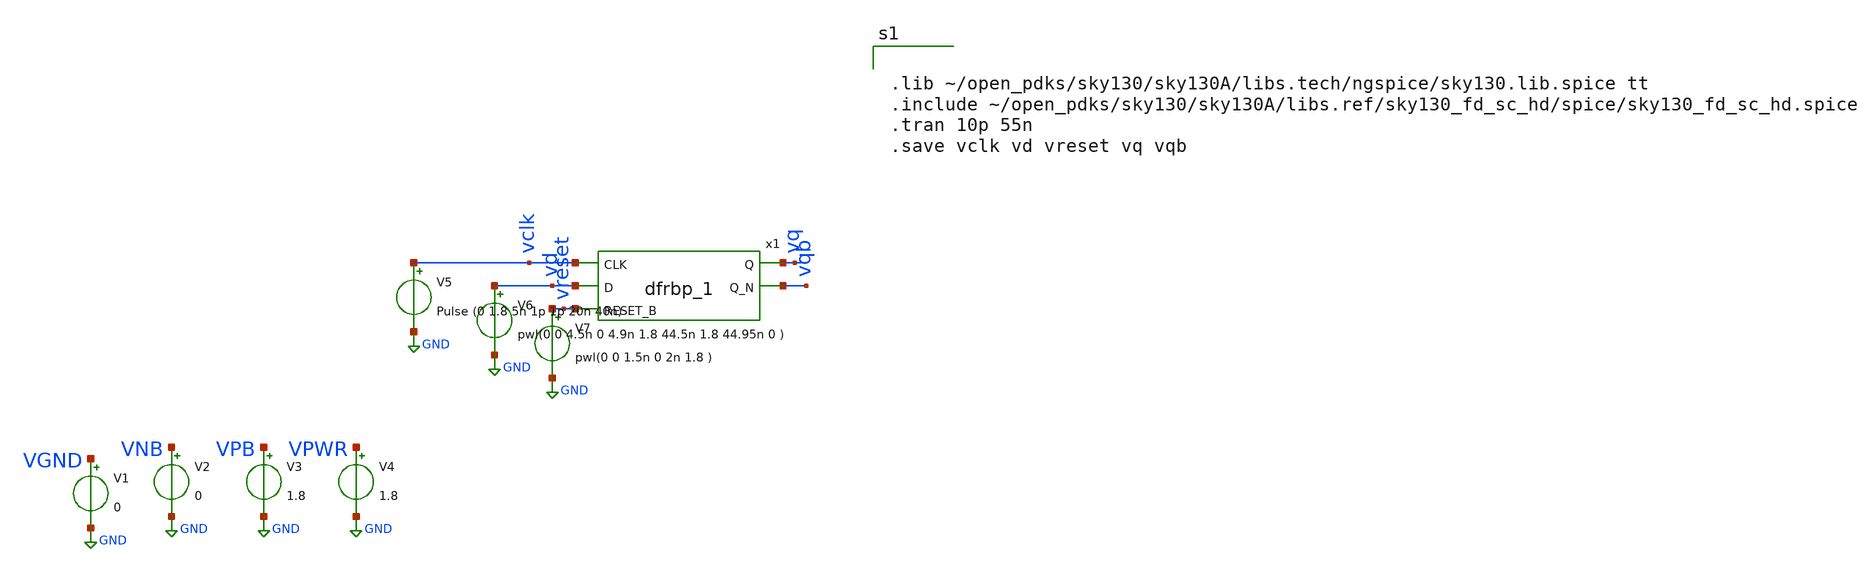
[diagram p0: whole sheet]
** sch_path: ff.sch
**.subckt ff
x1 vclk vd vreset VGND VNB VPB VPWR vq vqb sky130_fd_sc_hd__dfrbp_1
V1 VGND GND 0
V2 VNB GND 0
V3 VPB GND 1.8
V4 VPWR GND 1.8
V5 vclk GND Pulse (0 1.8 5n 1p 1p 20n 40n)
V6 vd GND pwl(0 0 4.5n 0 4.9n 1.8 44.5n 1.8 44.95n 0 )
V7 vreset GND pwl(0 0 1.5n 0 2n 1.8 )
**** begin user architecture code


.lib ~/open_pdks/sky130/sky130A/libs.tech/ngspice/sky130.lib.spice tt
.include ~/open_pdks/sky130/sky130A/libs.ref/sky130_fd_sc_hd/spice/sky130_fd_sc_hd.spice
.tran 10p 55n
.save vclk vd vreset vq vqb

**** end user architecture code
**.ends
.GLOBAL GND
.end
